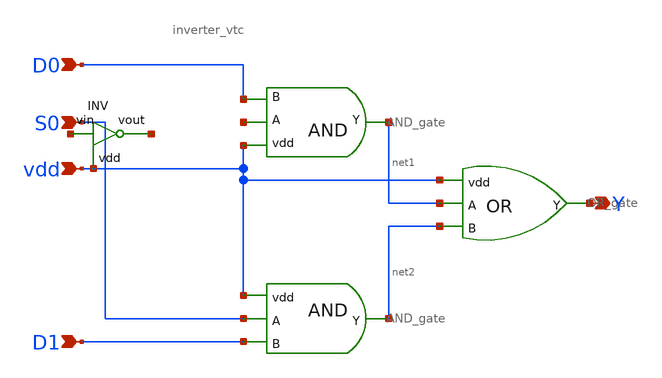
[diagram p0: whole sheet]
** sch_path: Circuit Files/circuits/circuits/2:1mux.sch
**.subckt 2:1mux vdd D1 D0 S0 Y
*.ipin vdd
*.ipin D1
*.ipin D0
*.ipin S0
*.opin Y
x1 vdd net3 net1 D0 AND_gate
x2 vdd net1 net2 Y OR_gate
x3 vdd net4 net5 inverter_vtc
x4 vdd S0 net2 D1 AND_gate
**.ends

* expanding   symbol:  daVLSI_World/gates/AND_gate.sym # of pins=4
** sym_path: Circuit Files/Logic gate design using MOSFETS/gates/AND_gate.sym
** sch_path: Circuit Files/Logic gate design using MOSFETS/gates/AND_gate.sch
.subckt AND_gate vdd A Y B
*.opin Y
*.ipin A
*.ipin B
*.ipin vdd
x1 vdd net1 A B GND NAND_gate
x2 vdd net1 Y inverter_vtc
.ends


* expanding   symbol:  daVLSI_World/gates/OR_gate.sym # of pins=4
** sym_path: Circuit Files/Logic gate design using MOSFETS/gates/OR_gate.sym
** sch_path: Circuit Files/Logic gate design using MOSFETS/gates/OR_gate.sch
.subckt OR_gate vdd A B Y
*.ipin A
*.ipin B
*.ipin vdd
*.opin Y
XM1 net1 B net2 vdd sky130_fd_pr__pfet_01v8 L=0.15 W=2 nf=1 ad='int((nf+1)/2) * W/nf * 0.29' as='int((nf+2)/2) * W/nf * 0.29'
+ pd='2*int((nf+1)/2) * (W/nf + 0.29)' ps='2*int((nf+2)/2) * (W/nf + 0.29)' nrd='0.29 / W' nrs='0.29 / W'
+ sa=0 sb=0 sd=0 mult=1 m=1
XM2 net2 A vdd vdd sky130_fd_pr__pfet_01v8 L=0.15 W=2 nf=1 ad='int((nf+1)/2) * W/nf * 0.29' as='int((nf+2)/2) * W/nf * 0.29'
+ pd='2*int((nf+1)/2) * (W/nf + 0.29)' ps='2*int((nf+2)/2) * (W/nf + 0.29)' nrd='0.29 / W' nrs='0.29 / W'
+ sa=0 sb=0 sd=0 mult=1 m=1
XM3 net1 B GND GND sky130_fd_pr__nfet_01v8 L=0.15 W=1 nf=1 ad='int((nf+1)/2) * W/nf * 0.29' as='int((nf+2)/2) * W/nf * 0.29'
+ pd='2*int((nf+1)/2) * (W/nf + 0.29)' ps='2*int((nf+2)/2) * (W/nf + 0.29)' nrd='0.29 / W' nrs='0.29 / W'
+ sa=0 sb=0 sd=0 mult=1 m=1
XM4 net1 A GND GND sky130_fd_pr__nfet_01v8 L=0.15 W=1 nf=1 ad='int((nf+1)/2) * W/nf * 0.29' as='int((nf+2)/2) * W/nf * 0.29'
+ pd='2*int((nf+1)/2) * (W/nf + 0.29)' ps='2*int((nf+2)/2) * (W/nf + 0.29)' nrd='0.29 / W' nrs='0.29 / W'
+ sa=0 sb=0 sd=0 mult=1 m=1
XM9 Y net1 vdd vdd sky130_fd_pr__pfet_01v8 L=0.15 W=2 nf=1 ad='int((nf+1)/2) * W/nf * 0.29' as='int((nf+2)/2) * W/nf * 0.29'
+ pd='2*int((nf+1)/2) * (W/nf + 0.29)' ps='2*int((nf+2)/2) * (W/nf + 0.29)' nrd='0.29 / W' nrs='0.29 / W'
+ sa=0 sb=0 sd=0 mult=1 m=1
XM10 Y net1 GND GND sky130_fd_pr__nfet_01v8 L=0.15 W=1 nf=1 ad='int((nf+1)/2) * W/nf * 0.29' as='int((nf+2)/2) * W/nf * 0.29'
+ pd='2*int((nf+1)/2) * (W/nf + 0.29)' ps='2*int((nf+2)/2) * (W/nf + 0.29)' nrd='0.29 / W' nrs='0.29 / W'
+ sa=0 sb=0 sd=0 mult=1 m=1
.ends


* expanding   symbol:  daVLSI_World/gates/inverter_vtc.sym # of pins=3
** sym_path: Circuit Files/Logic gate design using MOSFETS/gates/inverter_vtc.sym
** sch_path: Circuit Files/Logic gate design using MOSFETS/gates/inverter_vtc.sch
.subckt inverter_vtc vdd vin vout
*.ipin vin
*.opin vout
*.ipin vdd
XM1 vout vin GND GND sky130_fd_pr__nfet_01v8 L=0.15 W=1 nf=1 ad='int((nf+1)/2) * W/nf * 0.29' as='int((nf+2)/2) * W/nf * 0.29'
+ pd='2*int((nf+1)/2) * (W/nf + 0.29)' ps='2*int((nf+2)/2) * (W/nf + 0.29)' nrd='0.29 / W' nrs='0.29 / W'
+ sa=0 sb=0 sd=0 mult=1 m=1
XM2 vout vin vdd vdd sky130_fd_pr__pfet_01v8 L=0.15 W=2 nf=1 ad='int((nf+1)/2) * W/nf * 0.29' as='int((nf+2)/2) * W/nf * 0.29'
+ pd='2*int((nf+1)/2) * (W/nf + 0.29)' ps='2*int((nf+2)/2) * (W/nf + 0.29)' nrd='0.29 / W' nrs='0.29 / W'
+ sa=0 sb=0 sd=0 mult=1 m=1
.ends


* expanding   symbol:  daVLSI_World/gates/NAND_gate.sym # of pins=5
** sym_path: Circuit Files/Logic gate design using MOSFETS/gates/NAND_gate.sym
** sch_path: Circuit Files/Logic gate design using MOSFETS/gates/NAND_gate.sch
.subckt NAND_gate vdd Y A B gnd
*.ipin A
*.ipin B
*.opin Y
*.ipin vdd
*.ipin gnd
XM1 Y A net1 gnd sky130_fd_pr__nfet_01v8 L=0.15 W=1 nf=1 ad='int((nf+1)/2) * W/nf * 0.29' as='int((nf+2)/2) * W/nf * 0.29'
+ pd='2*int((nf+1)/2) * (W/nf + 0.29)' ps='2*int((nf+2)/2) * (W/nf + 0.29)' nrd='0.29 / W' nrs='0.29 / W'
+ sa=0 sb=0 sd=0 mult=1 m=1
XM2 net1 B gnd gnd sky130_fd_pr__nfet_01v8 L=0.15 W=1 nf=1 ad='int((nf+1)/2) * W/nf * 0.29' as='int((nf+2)/2) * W/nf * 0.29'
+ pd='2*int((nf+1)/2) * (W/nf + 0.29)' ps='2*int((nf+2)/2) * (W/nf + 0.29)' nrd='0.29 / W' nrs='0.29 / W'
+ sa=0 sb=0 sd=0 mult=1 m=1
XM3 Y A vdd vdd sky130_fd_pr__pfet_01v8 L=0.15 W=2 nf=1 ad='int((nf+1)/2) * W/nf * 0.29' as='int((nf+2)/2) * W/nf * 0.29'
+ pd='2*int((nf+1)/2) * (W/nf + 0.29)' ps='2*int((nf+2)/2) * (W/nf + 0.29)' nrd='0.29 / W' nrs='0.29 / W'
+ sa=0 sb=0 sd=0 mult=1 m=1
XM4 Y B vdd vdd sky130_fd_pr__pfet_01v8 L=0.15 W=2 nf=1 ad='int((nf+1)/2) * W/nf * 0.29' as='int((nf+2)/2) * W/nf * 0.29'
+ pd='2*int((nf+1)/2) * (W/nf + 0.29)' ps='2*int((nf+2)/2) * (W/nf + 0.29)' nrd='0.29 / W' nrs='0.29 / W'
+ sa=0 sb=0 sd=0 mult=1 m=1
.ends

.GLOBAL GND
.end
